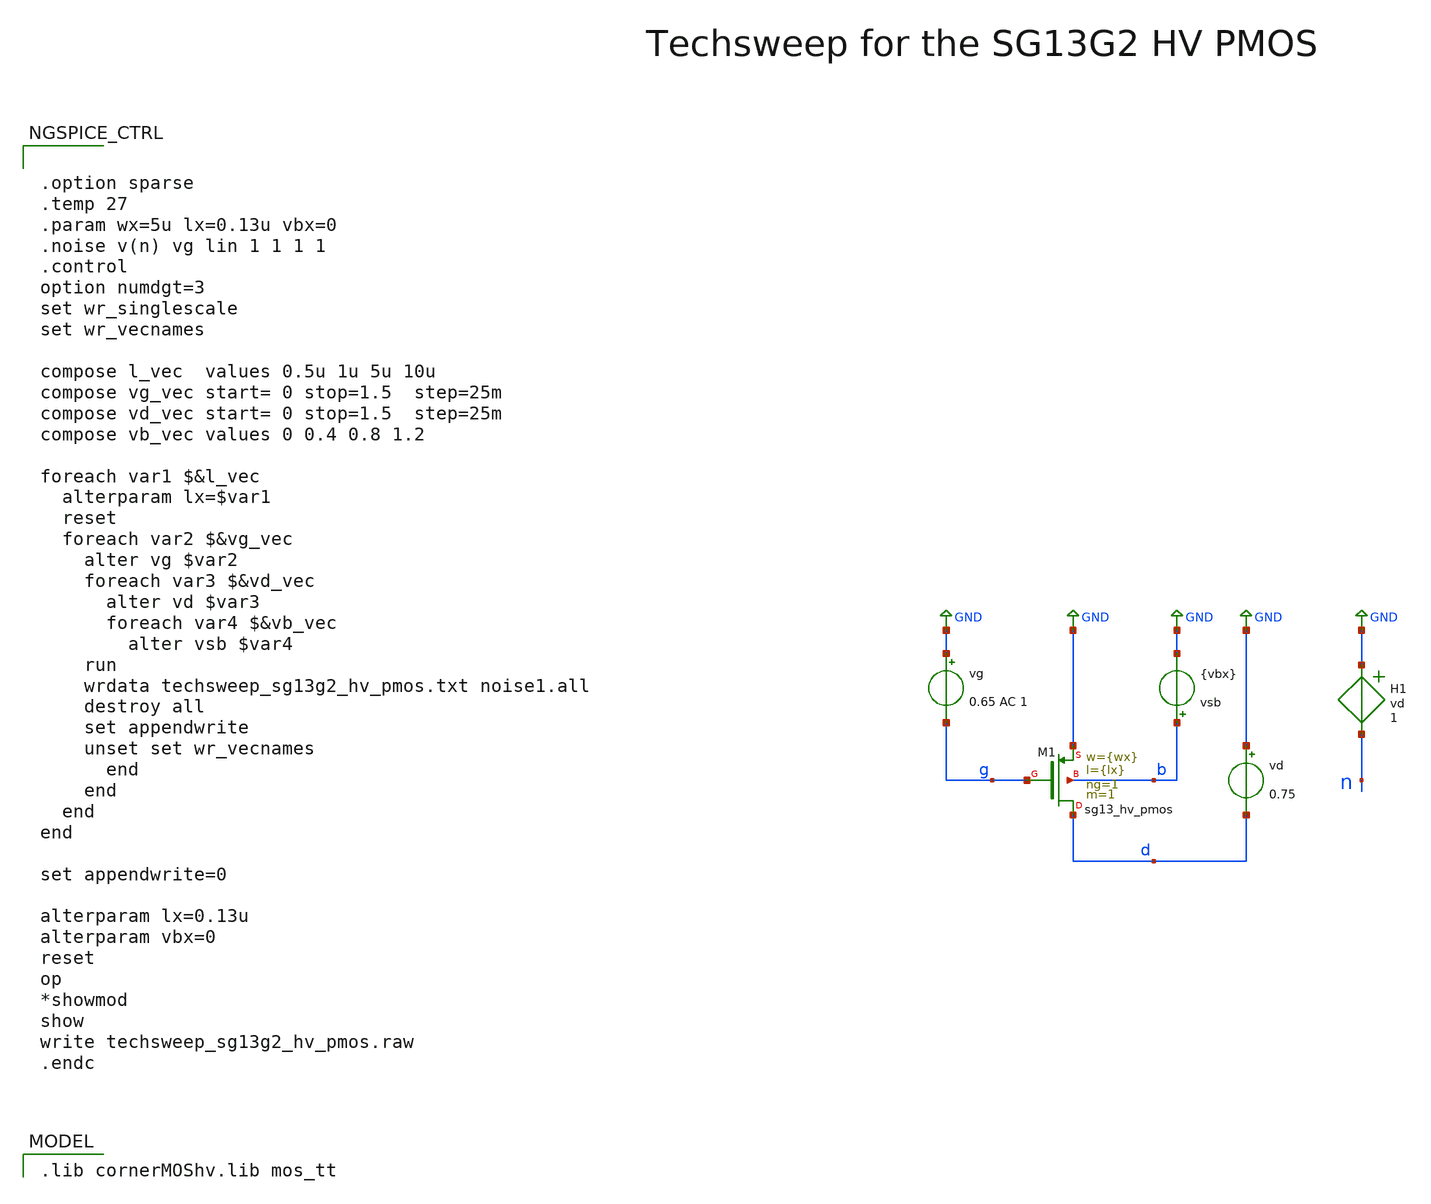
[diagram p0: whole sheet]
** sch_path: SG13G2_ATBS-ADC-main/xschem/techsweep/sg13g2_hv_pmos/techsweep_sg13g2_hv_pmos.sch
* (c) 2024 H. Pretl & S. Dorrer (adapted from B. Murmann)
**.subckt techsweep_sg13g2_hv_pmos
vd GND d 0.75
vsb b GND {vbx}
vg GND g 0.65 AC 1
H1 GND n vd 1
XM1 d g GND b sg13_hv_pmos w={wx} l={lx} ng=1 m=1 mm_ok=1
**** begin user architecture code
 .lib cornerMOShv.lib mos_tt



.save b d g n
.save @n.xm1.nsg13_hv_pmos[cgsol]
.save @n.xm1.nsg13_hv_pmos[cgdol]
.save @n.xm1.nsg13_hv_pmos[cdd]
.save @n.xm1.nsg13_hv_pmos[cgb]
.save @n.xm1.nsg13_hv_pmos[cgd]
.save @n.xm1.nsg13_hv_pmos[cgg]
.save @n.xm1.nsg13_hv_pmos[cgs]
.save @n.xm1.nsg13_hv_pmos[css]
.save @n.xm1.nsg13_hv_pmos[gds]
.save @n.xm1.nsg13_hv_pmos[gm]
.save @n.xm1.nsg13_hv_pmos[gmb]
.save @n.xm1.nsg13_hv_pmos[ids]
.save @n.xm1.nsg13_hv_pmos[l]
.save @n.xm1.nsg13_hv_pmos[vgs]
.save @n.xm1.nsg13_hv_pmos[vds]
.save @n.xm1.nsg13_hv_pmos[vsb]
.save @n.xm1.nsg13_hv_pmos[vth]
.save @n.xm1.nsg13_hv_pmos[vdss]
.save @n.xm1.nsg13_hv_pmos[fug]
.save @n.xm1.nsg13_hv_pmos[sid]
.save @n.xm1.nsg13_hv_pmos[sfl]
.save @n.xm1.nsg13_hv_pmos[cjd]
.save @n.xm1.nsg13_hv_pmos[cjs]
.save @n.xm1.nsg13_hv_pmos[rg]




.option sparse
.temp 27
.param wx=5u lx=0.13u vbx=0
.noise v(n) vg lin 1 1 1 1
.control
option numdgt=3
set wr_singlescale
set wr_vecnames

compose l_vec  values 0.5u 1u 5u 10u
compose vg_vec start= 0 stop=1.5  step=25m
compose vd_vec start= 0 stop=1.5  step=25m
compose vb_vec values 0 0.4 0.8 1.2

foreach var1 $&l_vec
  alterparam lx=$var1
  reset
  foreach var2 $&vg_vec
    alter vg $var2
    foreach var3 $&vd_vec
      alter vd $var3
      foreach var4 $&vb_vec
        alter vsb $var4
	run
	wrdata techsweep_sg13g2_hv_pmos.txt noise1.all
	destroy all
	set appendwrite
	unset set wr_vecnames
      end
    end
  end
end

set appendwrite=0

alterparam lx=0.13u
alterparam vbx=0
reset
op
*showmod
show
write techsweep_sg13g2_hv_pmos.raw
.endc


**** end user architecture code
**.ends
.GLOBAL GND
.end
